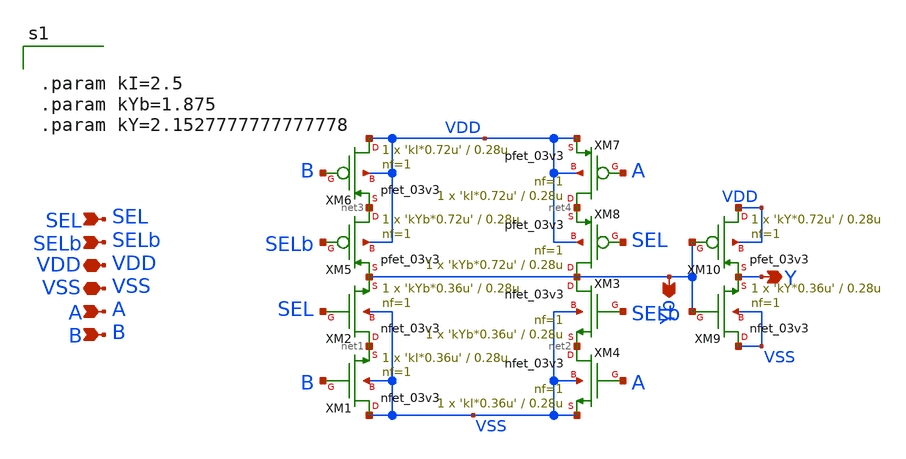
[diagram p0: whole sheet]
** sch_path: CAD4/2x1_mux_cmos.sch
**.subckt 2x1_mux_cmos A B SEL Y VDD VSS SELb Yb
*.ipin A
*.ipin B
*.ipin SEL
*.opin Y
*.iopin VDD
*.iopin VSS
*.ipin SELb
*.opin Yb
XM1 VSS B net1 VSS nfet_03v3 L=0.28u W='kI*0.36u' nf=1 ad='int((nf+1)/2) * W/nf * 0.18u' as='int((nf+2)/2) * W/nf * 0.18u'
+ pd='2*int((nf+1)/2) * (W/nf + 0.18u)' ps='2*int((nf+2)/2) * (W/nf + 0.18u)' nrd='0.18u / W' nrs='0.18u / W'
+ sa=0 sb=0 sd=0 m=1
XM2 net1 SEL Yb VSS nfet_03v3 L=0.28u W='kYb*0.36u' nf=1 ad='int((nf+1)/2) * W/nf * 0.18u' as='int((nf+2)/2) * W/nf * 0.18u'
+ pd='2*int((nf+1)/2) * (W/nf + 0.18u)' ps='2*int((nf+2)/2) * (W/nf + 0.18u)' nrd='0.18u / W' nrs='0.18u / W'
+ sa=0 sb=0 sd=0 m=1
XM3 Yb SELb net2 VSS nfet_03v3 L=0.28u W='kYb*0.36u' nf=1 ad='int((nf+1)/2) * W/nf * 0.18u' as='int((nf+2)/2) * W/nf * 0.18u'
+ pd='2*int((nf+1)/2) * (W/nf + 0.18u)' ps='2*int((nf+2)/2) * (W/nf + 0.18u)' nrd='0.18u / W' nrs='0.18u / W'
+ sa=0 sb=0 sd=0 m=1
XM4 net2 A VSS VSS nfet_03v3 L=0.28u W='kI*0.36u' nf=1 ad='int((nf+1)/2) * W/nf * 0.18u' as='int((nf+2)/2) * W/nf * 0.18u'
+ pd='2*int((nf+1)/2) * (W/nf + 0.18u)' ps='2*int((nf+2)/2) * (W/nf + 0.18u)' nrd='0.18u / W' nrs='0.18u / W'
+ sa=0 sb=0 sd=0 m=1
XM5 net3 SELb Yb VDD pfet_03v3 L=0.28u W='kYb*0.72u' nf=1 ad='int((nf+1)/2) * W/nf * 0.18u' as='int((nf+2)/2) * W/nf * 0.18u'
+ pd='2*int((nf+1)/2) * (W/nf + 0.18u)' ps='2*int((nf+2)/2) * (W/nf + 0.18u)' nrd='0.18u / W' nrs='0.18u / W'
+ sa=0 sb=0 sd=0 m=1
XM6 VDD B net3 VDD pfet_03v3 L=0.28u W='kI*0.72u' nf=1 ad='int((nf+1)/2) * W/nf * 0.18u' as='int((nf+2)/2) * W/nf * 0.18u'
+ pd='2*int((nf+1)/2) * (W/nf + 0.18u)' ps='2*int((nf+2)/2) * (W/nf + 0.18u)' nrd='0.18u / W' nrs='0.18u / W'
+ sa=0 sb=0 sd=0 m=1
XM7 net4 A VDD VDD pfet_03v3 L=0.28u W='kI*0.72u' nf=1 ad='int((nf+1)/2) * W/nf * 0.18u' as='int((nf+2)/2) * W/nf * 0.18u'
+ pd='2*int((nf+1)/2) * (W/nf + 0.18u)' ps='2*int((nf+2)/2) * (W/nf + 0.18u)' nrd='0.18u / W' nrs='0.18u / W'
+ sa=0 sb=0 sd=0 m=1
XM8 Yb SEL net4 VDD pfet_03v3 L=0.28u W='kYb*0.72u' nf=1 ad='int((nf+1)/2) * W/nf * 0.18u' as='int((nf+2)/2) * W/nf * 0.18u'
+ pd='2*int((nf+1)/2) * (W/nf + 0.18u)' ps='2*int((nf+2)/2) * (W/nf + 0.18u)' nrd='0.18u / W' nrs='0.18u / W'
+ sa=0 sb=0 sd=0 m=1
XM9 VSS Yb Y VSS nfet_03v3 L=0.28u W='kY*0.36u' nf=1 ad='int((nf+1)/2) * W/nf * 0.18u' as='int((nf+2)/2) * W/nf * 0.18u'
+ pd='2*int((nf+1)/2) * (W/nf + 0.18u)' ps='2*int((nf+2)/2) * (W/nf + 0.18u)' nrd='0.18u / W' nrs='0.18u / W'
+ sa=0 sb=0 sd=0 m=1
XM10 VDD Yb Y VDD pfet_03v3 L=0.28u W='kY*0.72u' nf=1 ad='int((nf+1)/2) * W/nf * 0.18u' as='int((nf+2)/2) * W/nf * 0.18u'
+ pd='2*int((nf+1)/2) * (W/nf + 0.18u)' ps='2*int((nf+2)/2) * (W/nf + 0.18u)' nrd='0.18u / W' nrs='0.18u / W'
+ sa=0 sb=0 sd=0 m=1
**** begin user architecture code


.param kI=2.5
.param kYb=1.875
.param kY=2.1527777777777778


**** end user architecture code
**.ends
.end
